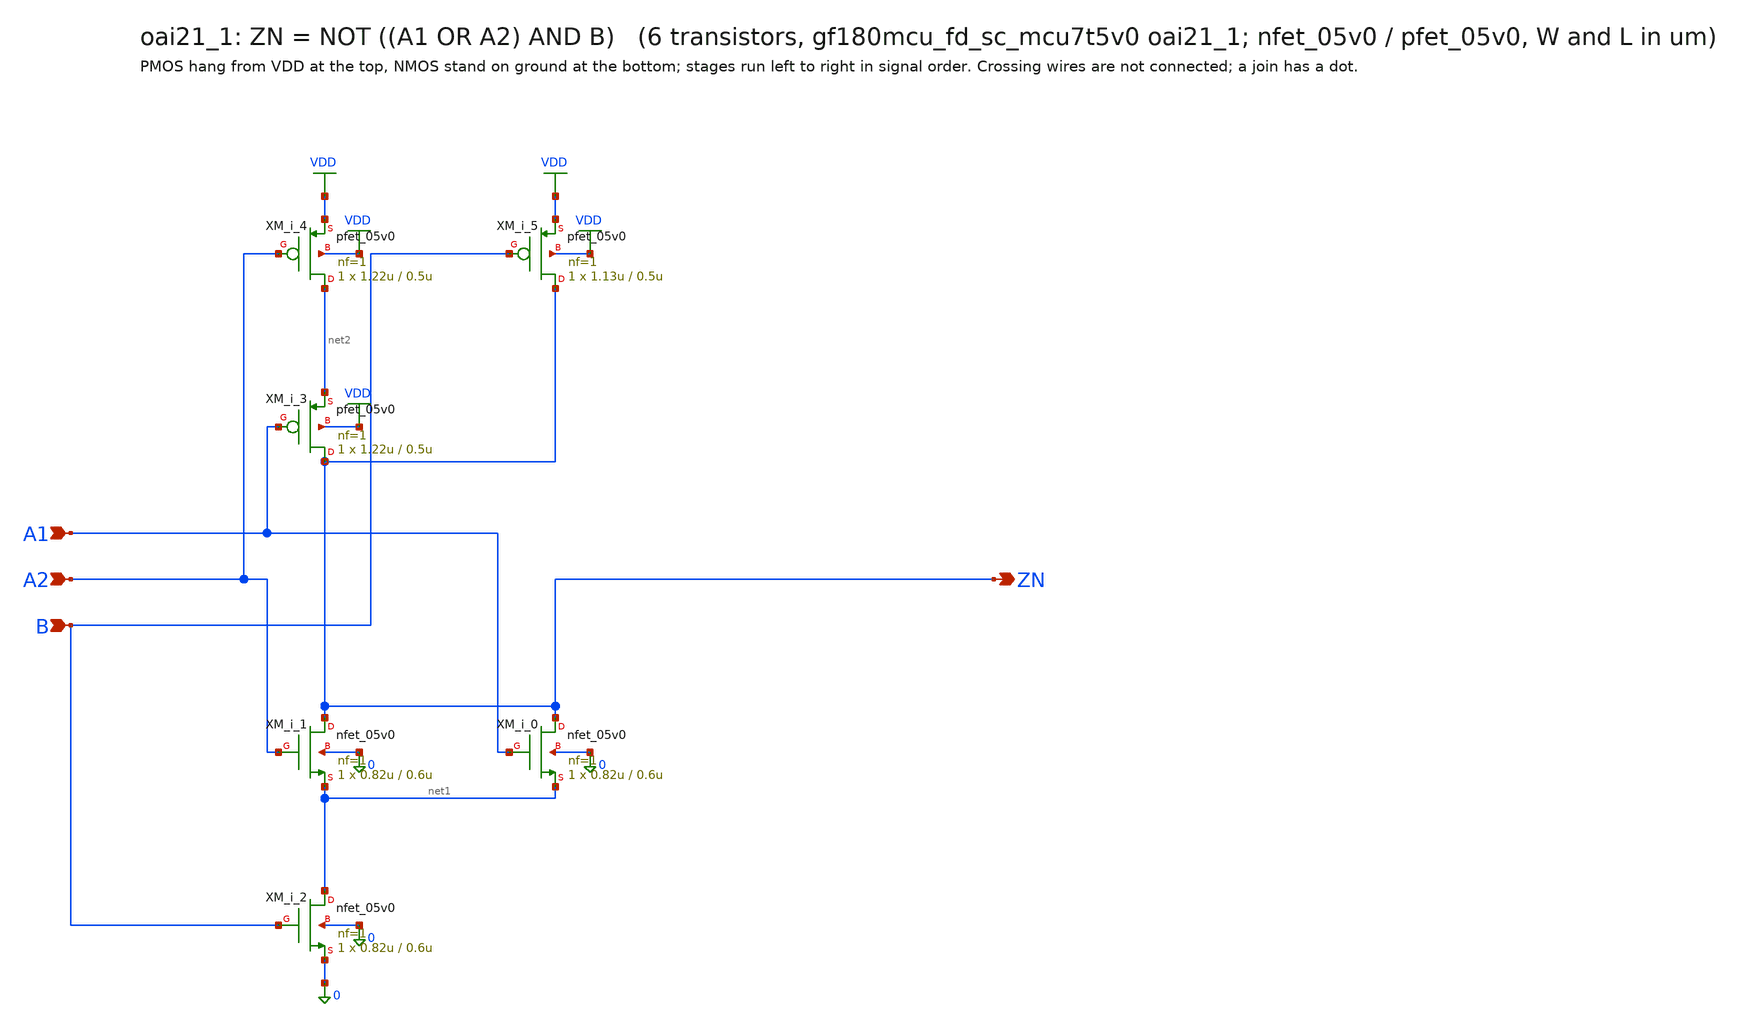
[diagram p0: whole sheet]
** sch_path: xschem/cells_tx/oai21_1.sch
**.subckt oai21_1 A1 A2 B ZN
*.ipin A1
*.ipin A2
*.ipin B
*.opin ZN
XM_i_1 ZN A2 net1 0 nfet_05v0 L=0.6u W=0.82u nf=1 ad=4.1e-13 as=4.1e-13 pd=2.64e-06 ps=2.64e-06
+ nrd=0 nrs=0 sa=0 sb=0 sd=0 m=1
XM_i_0 ZN A1 net1 0 nfet_05v0 L=0.6u W=0.82u nf=1 ad=4.1e-13 as=4.1e-13 pd=2.64e-06 ps=2.64e-06
+ nrd=0 nrs=0 sa=0 sb=0 sd=0 m=1
XM_i_2 net1 B 0 0 nfet_05v0 L=0.6u W=0.82u nf=1 ad=4.1e-13 as=4.1e-13 pd=2.64e-06 ps=2.64e-06 nrd=0
+ nrs=0 sa=0 sb=0 sd=0 m=1
XM_i_4 net2 A2 VDD VDD pfet_05v0 L=0.5u W=1.22u nf=1 ad=6.1e-13 as=6.1e-13 pd=3.44e-06 ps=3.44e-06
+ nrd=0 nrs=0 sa=0 sb=0 sd=0 m=1
XM_i_3 ZN A1 net2 VDD pfet_05v0 L=0.5u W=1.22u nf=1 ad=6.1e-13 as=6.1e-13 pd=3.44e-06 ps=3.44e-06
+ nrd=0 nrs=0 sa=0 sb=0 sd=0 m=1
XM_i_5 ZN B VDD VDD pfet_05v0 L=0.5u W=1.13u nf=1 ad=5.65e-13 as=5.65e-13 pd=3.26e-06 ps=3.26e-06
+ nrd=0 nrs=0 sa=0 sb=0 sd=0 m=1
**.ends
.GLOBAL VDD
.end
